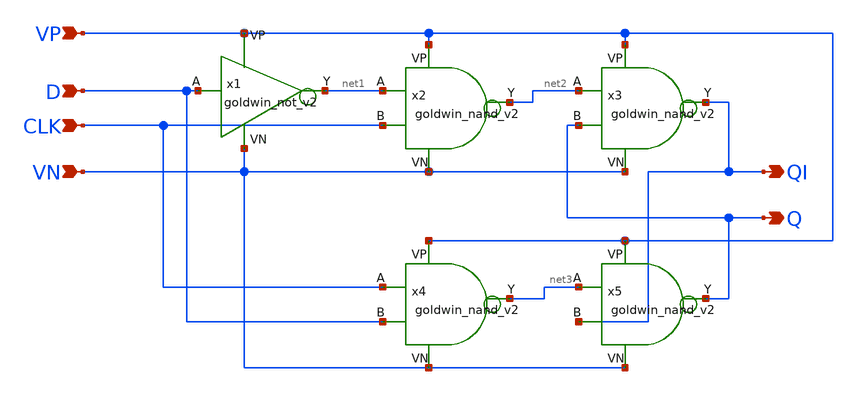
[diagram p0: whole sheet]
** sch_path: APIC-UTS/schematic/goldwin_dff_v2/goldwin_dff_v2.sch
**.subckt goldwin_dff_v2 D CLK VP VN Q QI
*.ipin D
*.ipin CLK
*.ipin VP
*.ipin VN
*.opin Q
*.opin QI
x1 D net1 VP VN goldwin_not_v2
x2 net1 CLK net2 VP VN goldwin_nand_v2
x3 net2 Q QI VP VN goldwin_nand_v2
x4 CLK D net3 VP VN goldwin_nand_v2
x5 net3 QI Q VP VN goldwin_nand_v2
**.ends
.end
